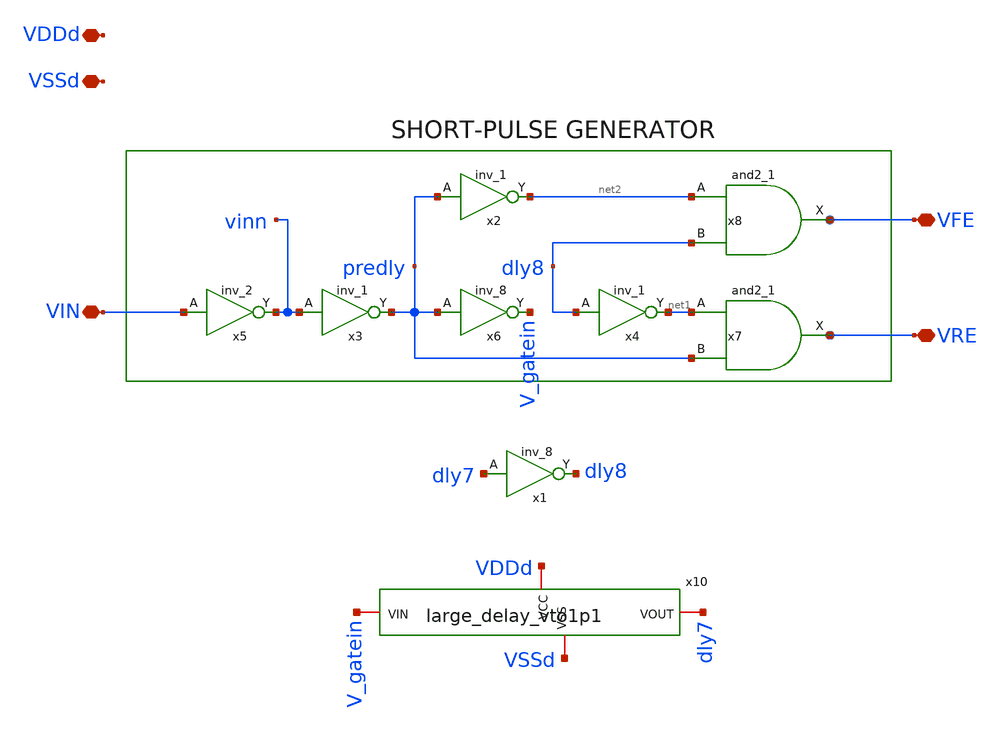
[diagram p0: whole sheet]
** sch_path: xschem/gf180_digital/SPG/SPG_vto1p1.sch
**.subckt SPG_vto1p1 VIN VFE VRE VDDd VSSd
*.iopin VIN
*.iopin VFE
*.iopin VRE
*.iopin VDDd
*.iopin VSSd
x2 predly VSSd VDDd VSSd VDDd net2 gf180mcu_fd_sc_mcu9t5v0__inv_1
x3 vinn VSSd VDDd VSSd VDDd predly gf180mcu_fd_sc_mcu9t5v0__inv_1
x4 dly8 VSSd VDDd VSSd VDDd net1 gf180mcu_fd_sc_mcu9t5v0__inv_1
x5 VIN VSSd VDDd VSSd VDDd vinn gf180mcu_fd_sc_mcu9t5v0__inv_2
x6 predly VSSd VDDd VSSd VDDd V_gatein gf180mcu_fd_sc_mcu9t5v0__inv_8
x1 dly7 VSSd VDDd VSSd VDDd dly8 gf180mcu_fd_sc_mcu9t5v0__inv_8
x8 net2 dly8 VSSd VDDd VSSd VDDd VFE gf180mcu_fd_sc_mcu9t5v0__and2_1
x7 net1 predly VSSd VDDd VSSd VDDd VRE gf180mcu_fd_sc_mcu9t5v0__and2_1
x10 VDDd VSSd V_gatein dly7 large_delay_vto1p1
**.ends
.end
